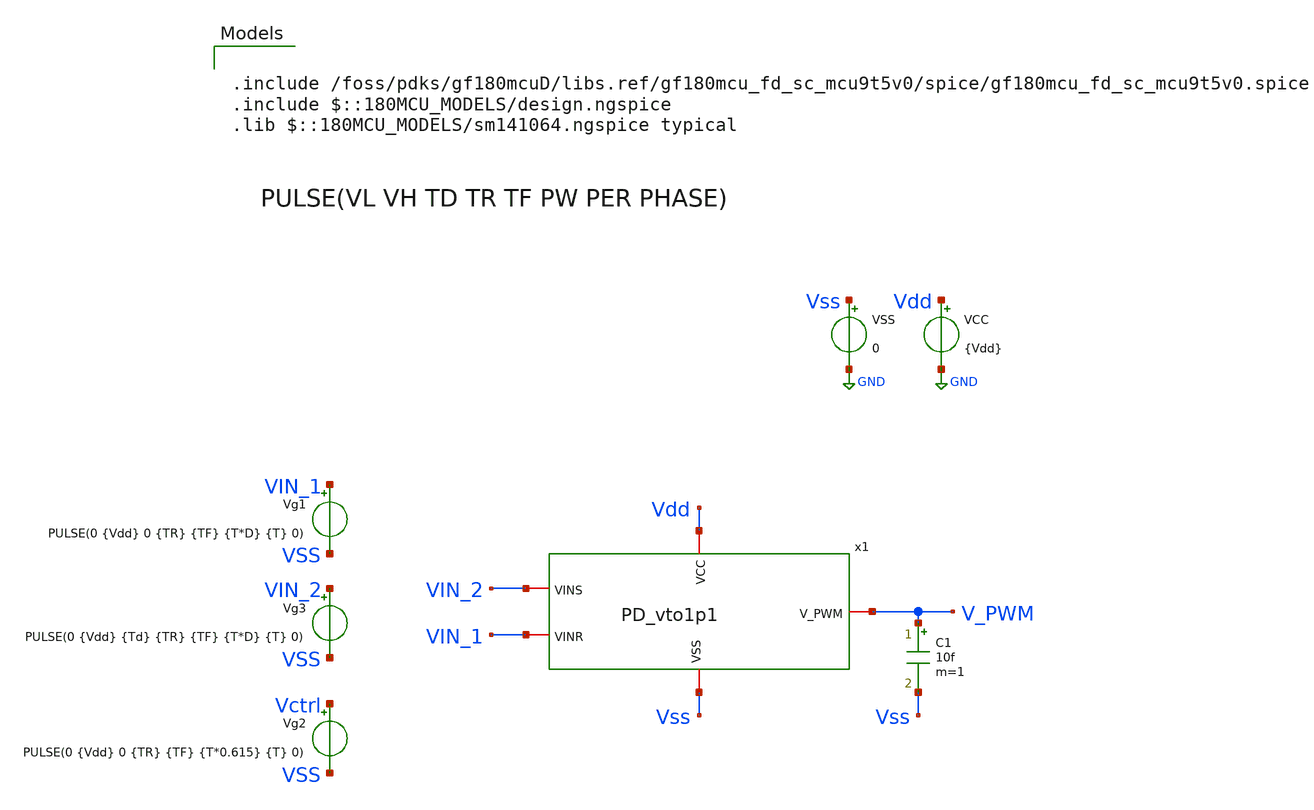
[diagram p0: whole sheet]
** sch_path: xschem/gf180_digital/PD/tb_PD_vto1p1.sch
**.subckt tb_PD_vto1p1
VCC Vdd GND {Vdd}
VSS Vss GND 0
Vg1 VIN_1 VSS PULSE(0 {Vdd} 0 {TR} {TF} {T*D} {T} 0)
C1 V_PWM Vss 10f m=1
Vg3 VIN_2 VSS PULSE(0 {Vdd} {Td} {TR} {TF} {T*D} {T} 0)
x1 Vdd Vss VIN_2 V_PWM VIN_1 PD_vto1p1
Vg2 Vctrl VSS PULSE(0 {Vdd} 0 {TR} {TF} {T*0.615} {T} 0)
**** begin user architecture code


.param Vdd = 5
.param VH = 5
.param Del = 0

.param T = 0.1u
.param TR = 1p
.param TF = 1p
.param DD = 0.615

*Caso 1 - No funciona bien
*.param D = 0.8
*.param Td = 0.03u

*Caso 2 - Funciona bien
*.param D = 0.5
*.param Td = DD*T

*Caso 3 - Funciona bien
*.param D = 0.615
*.param Td = 0.03u

*Caso 4 - No funciona bien
.param D = 0.615
.param Td = 0.08u




.param temp = 27





.save all

.control
set color0 = white
tran 100p 300n
plot v(VIN_1) v(VIN_2)+6 v(V_PWM)+12
plot v(V_PWM) v(Vctrl)+6
.endc

.measure tran tdead_fall  TRIG tran1.V(vcn) TD=0u VAL=0.6 FALL=1  TARG tran1.V(vcp) TD=0u VAL=0.6
+ FALL=1

.measure tran t_large_delay  TRIG tran1.V(x1.C1) TD=0u VAL=0.6 RISE=1  TARG tran1.V(x1.B2) TD=0u
+ VAL=0.6 RISE=1




.include /foss/pdks/gf180mcuD/libs.ref/gf180mcu_fd_sc_mcu9t5v0/spice/gf180mcu_fd_sc_mcu9t5v0.spice
.include $::180MCU_MODELS/design.ngspice
.lib $::180MCU_MODELS/sm141064.ngspice typical

**** end user architecture code
**.ends

* expanding   symbol:  gf180_digital/PD/PD_vto1p1.sym # of pins=5
** sym_path: xschem/gf180_digital/PD/PD_vto1p1.sym
** sch_path: xschem/gf180_digital/PD/PD_vto1p1.sch
.subckt PD_vto1p1 VCC VSS VINS V_PWM VINR
*.iopin V_PWM
*.iopin VCC
*.iopin VSS
*.iopin VINS
*.iopin VINR
C2 VFE1 VSS 100f m=1
C1 VFE1 VSS 100f m=1
x1 V_N net1 VSS VCC VSS VCC V_PWM gf180mcu_fd_sc_mcu9t5v0__nor2_1
x3 VCC VSS VFE1 VINR net2 SPG_vto1p1
x2 VCC VSS VFE1 VINS net1 SPG_vto1p1
x4 net2 V_PWM VSS VCC VSS VCC V_N gf180mcu_fd_sc_mcu9t5v0__nor2_1
.ends


* expanding   symbol:  gf180_digital/SPG/SPG_vto1p1.sym # of pins=5
** sym_path: xschem/gf180_digital/SPG/SPG_vto1p1.sym
** sch_path: xschem/gf180_digital/SPG/SPG_vto1p1.sch
.subckt SPG_vto1p1 VDDd VSSd VFE VIN VRE
*.iopin VIN
*.iopin VFE
*.iopin VRE
*.iopin VDDd
*.iopin VSSd
x2 predly VSSd VDDd VSSd VDDd net2 gf180mcu_fd_sc_mcu9t5v0__inv_1
x3 vinn VSSd VDDd VSSd VDDd predly gf180mcu_fd_sc_mcu9t5v0__inv_1
x4 dly8 VSSd VDDd VSSd VDDd net1 gf180mcu_fd_sc_mcu9t5v0__inv_1
x5 VIN VSSd VDDd VSSd VDDd vinn gf180mcu_fd_sc_mcu9t5v0__inv_2
x6 predly VSSd VDDd VSSd VDDd V_gatein gf180mcu_fd_sc_mcu9t5v0__inv_8
x9 VDDd VSSd V_gatein dly7 large_delay_vto1p1
x1 dly7 VSSd VDDd VSSd VDDd dly8 gf180mcu_fd_sc_mcu9t5v0__inv_8
x8 net2 dly8 VFE VDDd VDDd VSSd VSSd gf180mcu_fd_sc_mcu9t5v0__and2_1
x7 net1 predly VRE VDDd VDDd VSSd VSSd gf180mcu_fd_sc_mcu9t5v0__and2_1
.ends


* expanding   symbol:  gf180_digital/large_delay/large_delay_vto1p1.sym # of pins=4
** sym_path: xschem/gf180_digital/large_delay/large_delay_vto1p1.sym
** sch_path: xschem/gf180_digital/large_delay/large_delay_vto1p1.sch
.subckt large_delay_vto1p1 VDDd VSSd VIN VOUT
*.iopin VIN
*.iopin VOUT
*.iopin VDDd
*.iopin VSSd
x1 VIN VOUT VDDd VDDd VSSd VSSd gf180mcu_fd_sc_mcu9t5v0__dlya_1
.ends

.GLOBAL GND
.end
